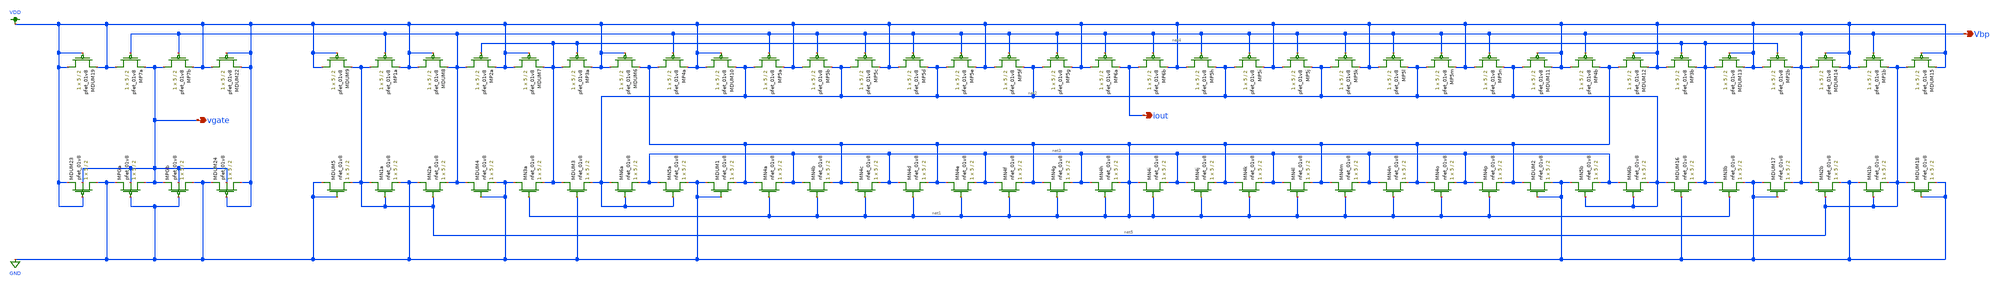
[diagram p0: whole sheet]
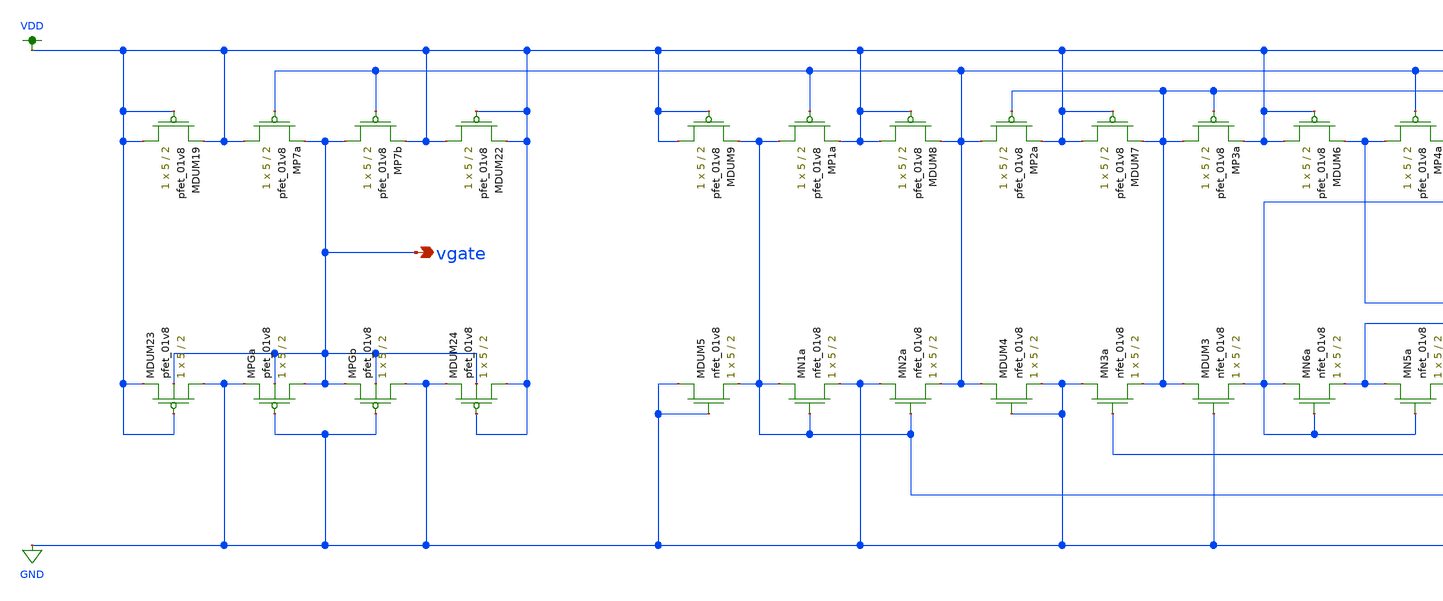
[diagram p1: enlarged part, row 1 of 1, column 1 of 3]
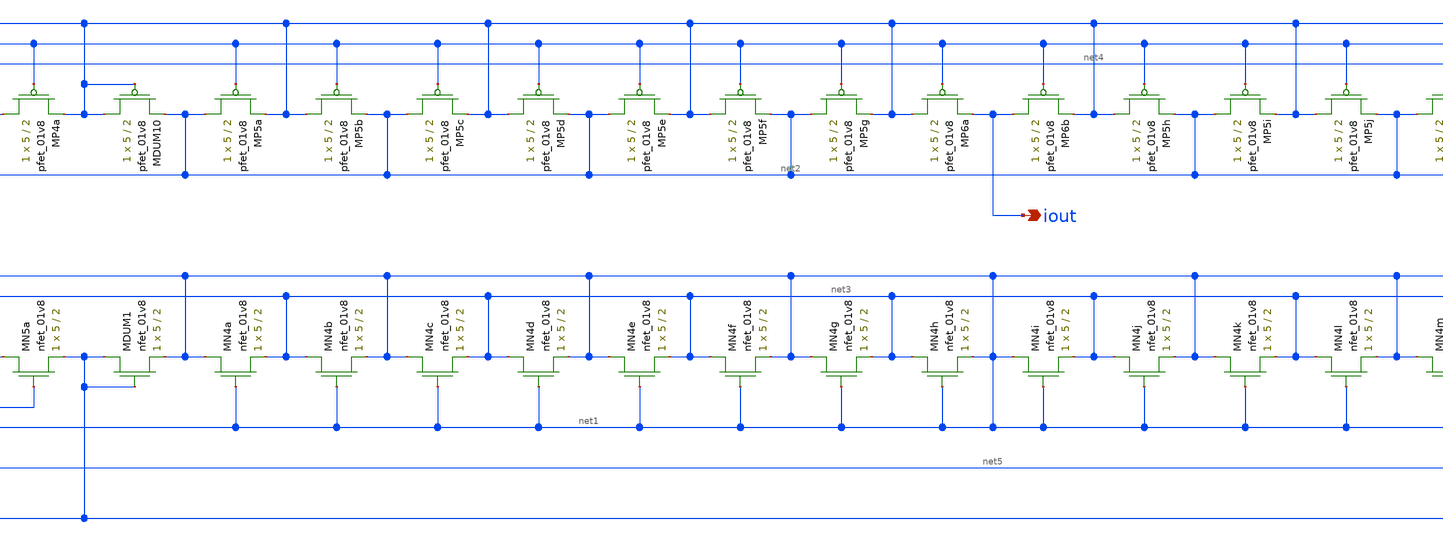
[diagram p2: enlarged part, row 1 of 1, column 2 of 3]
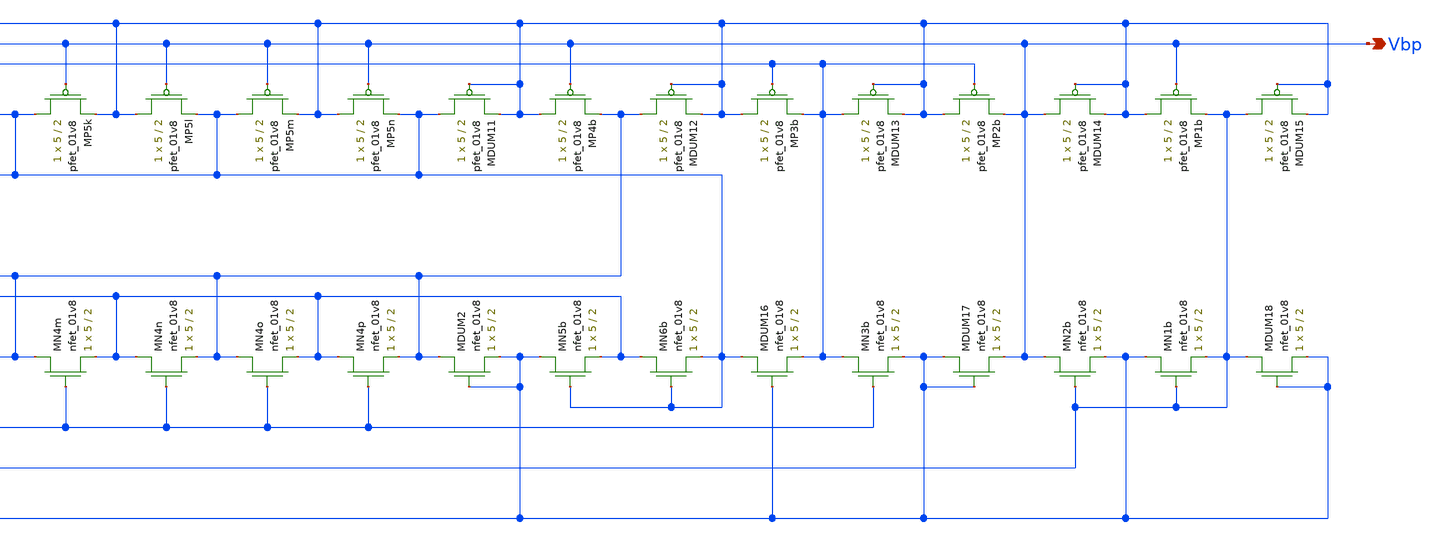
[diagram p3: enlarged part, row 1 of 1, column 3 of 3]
** sch_path: schematic/bias_current_LDS.sch
**.subckt bias_current_LDS iout Vbp vgate
*.opin iout
*.opin Vbp
*.opin vgate
XMP1a net5 Vbp VDD VDD sky130_fd_pr__pfet_01v8 L=2 W=5 nf=1 ad='int((nf+1)/2) * W/nf * 0.29' as='int((nf+2)/2) * W/nf * 0.29'
+ pd='2*int((nf+1)/2) * (W/nf + 0.29)' ps='2*int((nf+2)/2) * (W/nf + 0.29)' nrd='0.29 / W' nrs='0.29 / W'
+ sa=0 sb=0 sd=0 mult=1 m=1
XMP1b VDD Vbp net5 VDD sky130_fd_pr__pfet_01v8 L=2 W=5 nf=1 ad='int((nf+1)/2) * W/nf * 0.29' as='int((nf+2)/2) * W/nf * 0.29'
+ pd='2*int((nf+1)/2) * (W/nf + 0.29)' ps='2*int((nf+2)/2) * (W/nf + 0.29)' nrd='0.29 / W' nrs='0.29 / W'
+ sa=0 sb=0 sd=0 mult=1 m=1
XMP2a Vbp net4 VDD VDD sky130_fd_pr__pfet_01v8 L=2 W=5 nf=1 ad='int((nf+1)/2) * W/nf * 0.29' as='int((nf+2)/2) * W/nf * 0.29'
+ pd='2*int((nf+1)/2) * (W/nf + 0.29)' ps='2*int((nf+2)/2) * (W/nf + 0.29)' nrd='0.29 / W' nrs='0.29 / W'
+ sa=0 sb=0 sd=0 mult=1 m=1
XMP2b VDD net4 Vbp VDD sky130_fd_pr__pfet_01v8 L=2 W=5 nf=1 ad='int((nf+1)/2) * W/nf * 0.29' as='int((nf+2)/2) * W/nf * 0.29'
+ pd='2*int((nf+1)/2) * (W/nf + 0.29)' ps='2*int((nf+2)/2) * (W/nf + 0.29)' nrd='0.29 / W' nrs='0.29 / W'
+ sa=0 sb=0 sd=0 mult=1 m=1
XMP3a net4 net4 VDD VDD sky130_fd_pr__pfet_01v8 L=2 W=5 nf=1 ad='int((nf+1)/2) * W/nf * 0.29' as='int((nf+2)/2) * W/nf * 0.29'
+ pd='2*int((nf+1)/2) * (W/nf + 0.29)' ps='2*int((nf+2)/2) * (W/nf + 0.29)' nrd='0.29 / W' nrs='0.29 / W'
+ sa=0 sb=0 sd=0 mult=1 m=1
XMP3b VDD net4 net4 VDD sky130_fd_pr__pfet_01v8 L=2 W=5 nf=1 ad='int((nf+1)/2) * W/nf * 0.29' as='int((nf+2)/2) * W/nf * 0.29'
+ pd='2*int((nf+1)/2) * (W/nf + 0.29)' ps='2*int((nf+2)/2) * (W/nf + 0.29)' nrd='0.29 / W' nrs='0.29 / W'
+ sa=0 sb=0 sd=0 mult=1 m=1
XMP4a net1 Vbp VDD VDD sky130_fd_pr__pfet_01v8 L=2 W=5 nf=1 ad='int((nf+1)/2) * W/nf * 0.29' as='int((nf+2)/2) * W/nf * 0.29'
+ pd='2*int((nf+1)/2) * (W/nf + 0.29)' ps='2*int((nf+2)/2) * (W/nf + 0.29)' nrd='0.29 / W' nrs='0.29 / W'
+ sa=0 sb=0 sd=0 mult=1 m=1
XMP4b VDD Vbp net1 VDD sky130_fd_pr__pfet_01v8 L=2 W=5 nf=1 ad='int((nf+1)/2) * W/nf * 0.29' as='int((nf+2)/2) * W/nf * 0.29'
+ pd='2*int((nf+1)/2) * (W/nf + 0.29)' ps='2*int((nf+2)/2) * (W/nf + 0.29)' nrd='0.29 / W' nrs='0.29 / W'
+ sa=0 sb=0 sd=0 mult=1 m=1
XMN1a net5 net5 GND GND sky130_fd_pr__nfet_01v8 L=2 W=5 nf=1 ad='int((nf+1)/2) * W/nf * 0.29' as='int((nf+2)/2) * W/nf * 0.29'
+ pd='2*int((nf+1)/2) * (W/nf + 0.29)' ps='2*int((nf+2)/2) * (W/nf + 0.29)' nrd='0.29 / W' nrs='0.29 / W'
+ sa=0 sb=0 sd=0 mult=1 m=1
XMN1b GND net5 net5 GND sky130_fd_pr__nfet_01v8 L=2 W=5 nf=1 ad='int((nf+1)/2) * W/nf * 0.29' as='int((nf+2)/2) * W/nf * 0.29'
+ pd='2*int((nf+1)/2) * (W/nf + 0.29)' ps='2*int((nf+2)/2) * (W/nf + 0.29)' nrd='0.29 / W' nrs='0.29 / W'
+ sa=0 sb=0 sd=0 mult=1 m=1
XMN2a GND net5 Vbp GND sky130_fd_pr__nfet_01v8 L=2 W=5 nf=1 ad='int((nf+1)/2) * W/nf * 0.29' as='int((nf+2)/2) * W/nf * 0.29'
+ pd='2*int((nf+1)/2) * (W/nf + 0.29)' ps='2*int((nf+2)/2) * (W/nf + 0.29)' nrd='0.29 / W' nrs='0.29 / W'
+ sa=0 sb=0 sd=0 mult=1 m=1
XMN2b Vbp net5 GND GND sky130_fd_pr__nfet_01v8 L=2 W=5 nf=1 ad='int((nf+1)/2) * W/nf * 0.29' as='int((nf+2)/2) * W/nf * 0.29'
+ pd='2*int((nf+1)/2) * (W/nf + 0.29)' ps='2*int((nf+2)/2) * (W/nf + 0.29)' nrd='0.29 / W' nrs='0.29 / W'
+ sa=0 sb=0 sd=0 mult=1 m=1
XMN3a GND net1 net4 GND sky130_fd_pr__nfet_01v8 L=2 W=5 nf=1 ad='int((nf+1)/2) * W/nf * 0.29' as='int((nf+2)/2) * W/nf * 0.29'
+ pd='2*int((nf+1)/2) * (W/nf + 0.29)' ps='2*int((nf+2)/2) * (W/nf + 0.29)' nrd='0.29 / W' nrs='0.29 / W'
+ sa=0 sb=0 sd=0 mult=1 m=1
XMN3b net4 net1 GND GND sky130_fd_pr__nfet_01v8 L=2 W=5 nf=1 ad='int((nf+1)/2) * W/nf * 0.29' as='int((nf+2)/2) * W/nf * 0.29'
+ pd='2*int((nf+1)/2) * (W/nf + 0.29)' ps='2*int((nf+2)/2) * (W/nf + 0.29)' nrd='0.29 / W' nrs='0.29 / W'
+ sa=0 sb=0 sd=0 mult=1 m=1
XMN5a net3 net2 GND GND sky130_fd_pr__nfet_01v8 L=2 W=5 nf=1 ad='int((nf+1)/2) * W/nf * 0.29' as='int((nf+2)/2) * W/nf * 0.29'
+ pd='2*int((nf+1)/2) * (W/nf + 0.29)' ps='2*int((nf+2)/2) * (W/nf + 0.29)' nrd='0.29 / W' nrs='0.29 / W'
+ sa=0 sb=0 sd=0 mult=1 m=1
XMN5b GND net2 net3 GND sky130_fd_pr__nfet_01v8 L=2 W=5 nf=1 ad='int((nf+1)/2) * W/nf * 0.29' as='int((nf+2)/2) * W/nf * 0.29'
+ pd='2*int((nf+1)/2) * (W/nf + 0.29)' ps='2*int((nf+2)/2) * (W/nf + 0.29)' nrd='0.29 / W' nrs='0.29 / W'
+ sa=0 sb=0 sd=0 mult=1 m=1
XMN6a net2 net2 net3 GND sky130_fd_pr__nfet_01v8 L=2 W=5 nf=1 ad='int((nf+1)/2) * W/nf * 0.29' as='int((nf+2)/2) * W/nf * 0.29'
+ pd='2*int((nf+1)/2) * (W/nf + 0.29)' ps='2*int((nf+2)/2) * (W/nf + 0.29)' nrd='0.29 / W' nrs='0.29 / W'
+ sa=0 sb=0 sd=0 mult=1 m=1
XMN6b net3 net2 net2 GND sky130_fd_pr__nfet_01v8 L=2 W=5 nf=1 ad='int((nf+1)/2) * W/nf * 0.29' as='int((nf+2)/2) * W/nf * 0.29'
+ pd='2*int((nf+1)/2) * (W/nf + 0.29)' ps='2*int((nf+2)/2) * (W/nf + 0.29)' nrd='0.29 / W' nrs='0.29 / W'
+ sa=0 sb=0 sd=0 mult=1 m=1
XMP5g net2 Vbp VDD VDD sky130_fd_pr__pfet_01v8 L=2 W=5 nf=1 ad='int((nf+1)/2) * W/nf * 0.29' as='int((nf+2)/2) * W/nf * 0.29'
+ pd='2*int((nf+1)/2) * (W/nf + 0.29)' ps='2*int((nf+2)/2) * (W/nf + 0.29)' nrd='0.29 / W' nrs='0.29 / W'
+ sa=0 sb=0 sd=0 mult=1 m=1
XMP5h VDD Vbp net2 VDD sky130_fd_pr__pfet_01v8 L=2 W=5 nf=1 ad='int((nf+1)/2) * W/nf * 0.29' as='int((nf+2)/2) * W/nf * 0.29'
+ pd='2*int((nf+1)/2) * (W/nf + 0.29)' ps='2*int((nf+2)/2) * (W/nf + 0.29)' nrd='0.29 / W' nrs='0.29 / W'
+ sa=0 sb=0 sd=0 mult=1 m=1
XMP5a net2 Vbp VDD VDD sky130_fd_pr__pfet_01v8 L=2 W=5 nf=1 ad='int((nf+1)/2) * W/nf * 0.29' as='int((nf+2)/2) * W/nf * 0.29'
+ pd='2*int((nf+1)/2) * (W/nf + 0.29)' ps='2*int((nf+2)/2) * (W/nf + 0.29)' nrd='0.29 / W' nrs='0.29 / W'
+ sa=0 sb=0 sd=0 mult=1 m=1
XMP5b VDD Vbp net2 VDD sky130_fd_pr__pfet_01v8 L=2 W=5 nf=1 ad='int((nf+1)/2) * W/nf * 0.29' as='int((nf+2)/2) * W/nf * 0.29'
+ pd='2*int((nf+1)/2) * (W/nf + 0.29)' ps='2*int((nf+2)/2) * (W/nf + 0.29)' nrd='0.29 / W' nrs='0.29 / W'
+ sa=0 sb=0 sd=0 mult=1 m=1
XMP5c net2 Vbp VDD VDD sky130_fd_pr__pfet_01v8 L=2 W=5 nf=1 ad='int((nf+1)/2) * W/nf * 0.29' as='int((nf+2)/2) * W/nf * 0.29'
+ pd='2*int((nf+1)/2) * (W/nf + 0.29)' ps='2*int((nf+2)/2) * (W/nf + 0.29)' nrd='0.29 / W' nrs='0.29 / W'
+ sa=0 sb=0 sd=0 mult=1 m=1
XMP5d VDD Vbp net2 VDD sky130_fd_pr__pfet_01v8 L=2 W=5 nf=1 ad='int((nf+1)/2) * W/nf * 0.29' as='int((nf+2)/2) * W/nf * 0.29'
+ pd='2*int((nf+1)/2) * (W/nf + 0.29)' ps='2*int((nf+2)/2) * (W/nf + 0.29)' nrd='0.29 / W' nrs='0.29 / W'
+ sa=0 sb=0 sd=0 mult=1 m=1
XMP5e net2 Vbp VDD VDD sky130_fd_pr__pfet_01v8 L=2 W=5 nf=1 ad='int((nf+1)/2) * W/nf * 0.29' as='int((nf+2)/2) * W/nf * 0.29'
+ pd='2*int((nf+1)/2) * (W/nf + 0.29)' ps='2*int((nf+2)/2) * (W/nf + 0.29)' nrd='0.29 / W' nrs='0.29 / W'
+ sa=0 sb=0 sd=0 mult=1 m=1
XMP5f VDD Vbp net2 VDD sky130_fd_pr__pfet_01v8 L=2 W=5 nf=1 ad='int((nf+1)/2) * W/nf * 0.29' as='int((nf+2)/2) * W/nf * 0.29'
+ pd='2*int((nf+1)/2) * (W/nf + 0.29)' ps='2*int((nf+2)/2) * (W/nf + 0.29)' nrd='0.29 / W' nrs='0.29 / W'
+ sa=0 sb=0 sd=0 mult=1 m=1
XMP5i net2 Vbp VDD VDD sky130_fd_pr__pfet_01v8 L=2 W=5 nf=1 ad='int((nf+1)/2) * W/nf * 0.29' as='int((nf+2)/2) * W/nf * 0.29'
+ pd='2*int((nf+1)/2) * (W/nf + 0.29)' ps='2*int((nf+2)/2) * (W/nf + 0.29)' nrd='0.29 / W' nrs='0.29 / W'
+ sa=0 sb=0 sd=0 mult=1 m=1
XMP5j VDD Vbp net2 VDD sky130_fd_pr__pfet_01v8 L=2 W=5 nf=1 ad='int((nf+1)/2) * W/nf * 0.29' as='int((nf+2)/2) * W/nf * 0.29'
+ pd='2*int((nf+1)/2) * (W/nf + 0.29)' ps='2*int((nf+2)/2) * (W/nf + 0.29)' nrd='0.29 / W' nrs='0.29 / W'
+ sa=0 sb=0 sd=0 mult=1 m=1
XMP5k net2 Vbp VDD VDD sky130_fd_pr__pfet_01v8 L=2 W=5 nf=1 ad='int((nf+1)/2) * W/nf * 0.29' as='int((nf+2)/2) * W/nf * 0.29'
+ pd='2*int((nf+1)/2) * (W/nf + 0.29)' ps='2*int((nf+2)/2) * (W/nf + 0.29)' nrd='0.29 / W' nrs='0.29 / W'
+ sa=0 sb=0 sd=0 mult=1 m=1
XMP5l VDD Vbp net2 VDD sky130_fd_pr__pfet_01v8 L=2 W=5 nf=1 ad='int((nf+1)/2) * W/nf * 0.29' as='int((nf+2)/2) * W/nf * 0.29'
+ pd='2*int((nf+1)/2) * (W/nf + 0.29)' ps='2*int((nf+2)/2) * (W/nf + 0.29)' nrd='0.29 / W' nrs='0.29 / W'
+ sa=0 sb=0 sd=0 mult=1 m=1
XMP5m net2 Vbp VDD VDD sky130_fd_pr__pfet_01v8 L=2 W=5 nf=1 ad='int((nf+1)/2) * W/nf * 0.29' as='int((nf+2)/2) * W/nf * 0.29'
+ pd='2*int((nf+1)/2) * (W/nf + 0.29)' ps='2*int((nf+2)/2) * (W/nf + 0.29)' nrd='0.29 / W' nrs='0.29 / W'
+ sa=0 sb=0 sd=0 mult=1 m=1
XMP5n VDD Vbp net2 VDD sky130_fd_pr__pfet_01v8 L=2 W=5 nf=1 ad='int((nf+1)/2) * W/nf * 0.29' as='int((nf+2)/2) * W/nf * 0.29'
+ pd='2*int((nf+1)/2) * (W/nf + 0.29)' ps='2*int((nf+2)/2) * (W/nf + 0.29)' nrd='0.29 / W' nrs='0.29 / W'
+ sa=0 sb=0 sd=0 mult=1 m=1
XMP7a VDD Vbp vgate VDD sky130_fd_pr__pfet_01v8 L=2 W=5 nf=1 ad='int((nf+1)/2) * W/nf * 0.29' as='int((nf+2)/2) * W/nf * 0.29'
+ pd='2*int((nf+1)/2) * (W/nf + 0.29)' ps='2*int((nf+2)/2) * (W/nf + 0.29)' nrd='0.29 / W' nrs='0.29 / W'
+ sa=0 sb=0 sd=0 mult=1 m=1
XMDUM1 GND GND net1 GND sky130_fd_pr__nfet_01v8 L=2 W=5 nf=1 ad='int((nf+1)/2) * W/nf * 0.29' as='int((nf+2)/2) * W/nf * 0.29'
+ pd='2*int((nf+1)/2) * (W/nf + 0.29)' ps='2*int((nf+2)/2) * (W/nf + 0.29)' nrd='0.29 / W' nrs='0.29 / W'
+ sa=0 sb=0 sd=0 mult=1 m=1
XMN4a net1 net1 net3 GND sky130_fd_pr__nfet_01v8 L=2 W=5 nf=1 ad='int((nf+1)/2) * W/nf * 0.29' as='int((nf+2)/2) * W/nf * 0.29'
+ pd='2*int((nf+1)/2) * (W/nf + 0.29)' ps='2*int((nf+2)/2) * (W/nf + 0.29)' nrd='0.29 / W' nrs='0.29 / W'
+ sa=0 sb=0 sd=0 mult=1 m=1
XMN4b net3 net1 net1 GND sky130_fd_pr__nfet_01v8 L=2 W=5 nf=1 ad='int((nf+1)/2) * W/nf * 0.29' as='int((nf+2)/2) * W/nf * 0.29'
+ pd='2*int((nf+1)/2) * (W/nf + 0.29)' ps='2*int((nf+2)/2) * (W/nf + 0.29)' nrd='0.29 / W' nrs='0.29 / W'
+ sa=0 sb=0 sd=0 mult=1 m=1
XMN4c net1 net1 net3 GND sky130_fd_pr__nfet_01v8 L=2 W=5 nf=1 ad='int((nf+1)/2) * W/nf * 0.29' as='int((nf+2)/2) * W/nf * 0.29'
+ pd='2*int((nf+1)/2) * (W/nf + 0.29)' ps='2*int((nf+2)/2) * (W/nf + 0.29)' nrd='0.29 / W' nrs='0.29 / W'
+ sa=0 sb=0 sd=0 mult=1 m=1
XMN4d net3 net1 net1 GND sky130_fd_pr__nfet_01v8 L=2 W=5 nf=1 ad='int((nf+1)/2) * W/nf * 0.29' as='int((nf+2)/2) * W/nf * 0.29'
+ pd='2*int((nf+1)/2) * (W/nf + 0.29)' ps='2*int((nf+2)/2) * (W/nf + 0.29)' nrd='0.29 / W' nrs='0.29 / W'
+ sa=0 sb=0 sd=0 mult=1 m=1
XMN4e net1 net1 net3 GND sky130_fd_pr__nfet_01v8 L=2 W=5 nf=1 ad='int((nf+1)/2) * W/nf * 0.29' as='int((nf+2)/2) * W/nf * 0.29'
+ pd='2*int((nf+1)/2) * (W/nf + 0.29)' ps='2*int((nf+2)/2) * (W/nf + 0.29)' nrd='0.29 / W' nrs='0.29 / W'
+ sa=0 sb=0 sd=0 mult=1 m=1
XMN4f net3 net1 net1 GND sky130_fd_pr__nfet_01v8 L=2 W=5 nf=1 ad='int((nf+1)/2) * W/nf * 0.29' as='int((nf+2)/2) * W/nf * 0.29'
+ pd='2*int((nf+1)/2) * (W/nf + 0.29)' ps='2*int((nf+2)/2) * (W/nf + 0.29)' nrd='0.29 / W' nrs='0.29 / W'
+ sa=0 sb=0 sd=0 mult=1 m=1
XMN4i net1 net1 net3 GND sky130_fd_pr__nfet_01v8 L=2 W=5 nf=1 ad='int((nf+1)/2) * W/nf * 0.29' as='int((nf+2)/2) * W/nf * 0.29'
+ pd='2*int((nf+1)/2) * (W/nf + 0.29)' ps='2*int((nf+2)/2) * (W/nf + 0.29)' nrd='0.29 / W' nrs='0.29 / W'
+ sa=0 sb=0 sd=0 mult=1 m=1
XMN4g net1 net1 net3 GND sky130_fd_pr__nfet_01v8 L=2 W=5 nf=1 ad='int((nf+1)/2) * W/nf * 0.29' as='int((nf+2)/2) * W/nf * 0.29'
+ pd='2*int((nf+1)/2) * (W/nf + 0.29)' ps='2*int((nf+2)/2) * (W/nf + 0.29)' nrd='0.29 / W' nrs='0.29 / W'
+ sa=0 sb=0 sd=0 mult=1 m=1
XMN4h net3 net1 net1 GND sky130_fd_pr__nfet_01v8 L=2 W=5 nf=1 ad='int((nf+1)/2) * W/nf * 0.29' as='int((nf+2)/2) * W/nf * 0.29'
+ pd='2*int((nf+1)/2) * (W/nf + 0.29)' ps='2*int((nf+2)/2) * (W/nf + 0.29)' nrd='0.29 / W' nrs='0.29 / W'
+ sa=0 sb=0 sd=0 mult=1 m=1
XMN4j net3 net1 net1 GND sky130_fd_pr__nfet_01v8 L=2 W=5 nf=1 ad='int((nf+1)/2) * W/nf * 0.29' as='int((nf+2)/2) * W/nf * 0.29'
+ pd='2*int((nf+1)/2) * (W/nf + 0.29)' ps='2*int((nf+2)/2) * (W/nf + 0.29)' nrd='0.29 / W' nrs='0.29 / W'
+ sa=0 sb=0 sd=0 mult=1 m=1
XMN4k net1 net1 net3 GND sky130_fd_pr__nfet_01v8 L=2 W=5 nf=1 ad='int((nf+1)/2) * W/nf * 0.29' as='int((nf+2)/2) * W/nf * 0.29'
+ pd='2*int((nf+1)/2) * (W/nf + 0.29)' ps='2*int((nf+2)/2) * (W/nf + 0.29)' nrd='0.29 / W' nrs='0.29 / W'
+ sa=0 sb=0 sd=0 mult=1 m=1
XMN4l net3 net1 net1 GND sky130_fd_pr__nfet_01v8 L=2 W=5 nf=1 ad='int((nf+1)/2) * W/nf * 0.29' as='int((nf+2)/2) * W/nf * 0.29'
+ pd='2*int((nf+1)/2) * (W/nf + 0.29)' ps='2*int((nf+2)/2) * (W/nf + 0.29)' nrd='0.29 / W' nrs='0.29 / W'
+ sa=0 sb=0 sd=0 mult=1 m=1
XMN4m net1 net1 net3 GND sky130_fd_pr__nfet_01v8 L=2 W=5 nf=1 ad='int((nf+1)/2) * W/nf * 0.29' as='int((nf+2)/2) * W/nf * 0.29'
+ pd='2*int((nf+1)/2) * (W/nf + 0.29)' ps='2*int((nf+2)/2) * (W/nf + 0.29)' nrd='0.29 / W' nrs='0.29 / W'
+ sa=0 sb=0 sd=0 mult=1 m=1
XMN4p net3 net1 net1 GND sky130_fd_pr__nfet_01v8 L=2 W=5 nf=1 ad='int((nf+1)/2) * W/nf * 0.29' as='int((nf+2)/2) * W/nf * 0.29'
+ pd='2*int((nf+1)/2) * (W/nf + 0.29)' ps='2*int((nf+2)/2) * (W/nf + 0.29)' nrd='0.29 / W' nrs='0.29 / W'
+ sa=0 sb=0 sd=0 mult=1 m=1
XMN4n net3 net1 net1 GND sky130_fd_pr__nfet_01v8 L=2 W=5 nf=1 ad='int((nf+1)/2) * W/nf * 0.29' as='int((nf+2)/2) * W/nf * 0.29'
+ pd='2*int((nf+1)/2) * (W/nf + 0.29)' ps='2*int((nf+2)/2) * (W/nf + 0.29)' nrd='0.29 / W' nrs='0.29 / W'
+ sa=0 sb=0 sd=0 mult=1 m=1
XMN4o net1 net1 net3 GND sky130_fd_pr__nfet_01v8 L=2 W=5 nf=1 ad='int((nf+1)/2) * W/nf * 0.29' as='int((nf+2)/2) * W/nf * 0.29'
+ pd='2*int((nf+1)/2) * (W/nf + 0.29)' ps='2*int((nf+2)/2) * (W/nf + 0.29)' nrd='0.29 / W' nrs='0.29 / W'
+ sa=0 sb=0 sd=0 mult=1 m=1
XMDUM2 net1 GND GND GND sky130_fd_pr__nfet_01v8 L=2 W=5 nf=1 ad='int((nf+1)/2) * W/nf * 0.29' as='int((nf+2)/2) * W/nf * 0.29'
+ pd='2*int((nf+1)/2) * (W/nf + 0.29)' ps='2*int((nf+2)/2) * (W/nf + 0.29)' nrd='0.29 / W' nrs='0.29 / W'
+ sa=0 sb=0 sd=0 mult=1 m=1
XMDUM3 net4 GND net2 GND sky130_fd_pr__nfet_01v8 L=2 W=5 nf=1 ad='int((nf+1)/2) * W/nf * 0.29' as='int((nf+2)/2) * W/nf * 0.29'
+ pd='2*int((nf+1)/2) * (W/nf + 0.29)' ps='2*int((nf+2)/2) * (W/nf + 0.29)' nrd='0.29 / W' nrs='0.29 / W'
+ sa=0 sb=0 sd=0 mult=1 m=1
XMDUM4 Vbp GND GND GND sky130_fd_pr__nfet_01v8 L=2 W=5 nf=1 ad='int((nf+1)/2) * W/nf * 0.29' as='int((nf+2)/2) * W/nf * 0.29'
+ pd='2*int((nf+1)/2) * (W/nf + 0.29)' ps='2*int((nf+2)/2) * (W/nf + 0.29)' nrd='0.29 / W' nrs='0.29 / W'
+ sa=0 sb=0 sd=0 mult=1 m=1
XMDUM5 GND GND net5 GND sky130_fd_pr__nfet_01v8 L=2 W=5 nf=1 ad='int((nf+1)/2) * W/nf * 0.29' as='int((nf+2)/2) * W/nf * 0.29'
+ pd='2*int((nf+1)/2) * (W/nf + 0.29)' ps='2*int((nf+2)/2) * (W/nf + 0.29)' nrd='0.29 / W' nrs='0.29 / W'
+ sa=0 sb=0 sd=0 mult=1 m=1
XMDUM6 VDD VDD net1 VDD sky130_fd_pr__pfet_01v8 L=2 W=5 nf=1 ad='int((nf+1)/2) * W/nf * 0.29' as='int((nf+2)/2) * W/nf * 0.29'
+ pd='2*int((nf+1)/2) * (W/nf + 0.29)' ps='2*int((nf+2)/2) * (W/nf + 0.29)' nrd='0.29 / W' nrs='0.29 / W'
+ sa=0 sb=0 sd=0 mult=1 m=1
XMDUM7 VDD VDD net4 VDD sky130_fd_pr__pfet_01v8 L=2 W=5 nf=1 ad='int((nf+1)/2) * W/nf * 0.29' as='int((nf+2)/2) * W/nf * 0.29'
+ pd='2*int((nf+1)/2) * (W/nf + 0.29)' ps='2*int((nf+2)/2) * (W/nf + 0.29)' nrd='0.29 / W' nrs='0.29 / W'
+ sa=0 sb=0 sd=0 mult=1 m=1
XMDUM8 VDD VDD Vbp VDD sky130_fd_pr__pfet_01v8 L=2 W=5 nf=1 ad='int((nf+1)/2) * W/nf * 0.29' as='int((nf+2)/2) * W/nf * 0.29'
+ pd='2*int((nf+1)/2) * (W/nf + 0.29)' ps='2*int((nf+2)/2) * (W/nf + 0.29)' nrd='0.29 / W' nrs='0.29 / W'
+ sa=0 sb=0 sd=0 mult=1 m=1
XMDUM9 VDD VDD net5 VDD sky130_fd_pr__pfet_01v8 L=2 W=5 nf=1 ad='int((nf+1)/2) * W/nf * 0.29' as='int((nf+2)/2) * W/nf * 0.29'
+ pd='2*int((nf+1)/2) * (W/nf + 0.29)' ps='2*int((nf+2)/2) * (W/nf + 0.29)' nrd='0.29 / W' nrs='0.29 / W'
+ sa=0 sb=0 sd=0 mult=1 m=1
XMDUM10 VDD VDD net2 VDD sky130_fd_pr__pfet_01v8 L=2 W=5 nf=1 ad='int((nf+1)/2) * W/nf * 0.29' as='int((nf+2)/2) * W/nf * 0.29'
+ pd='2*int((nf+1)/2) * (W/nf + 0.29)' ps='2*int((nf+2)/2) * (W/nf + 0.29)' nrd='0.29 / W' nrs='0.29 / W'
+ sa=0 sb=0 sd=0 mult=1 m=1
XMDUM11 net2 VDD VDD VDD sky130_fd_pr__pfet_01v8 L=2 W=5 nf=1 ad='int((nf+1)/2) * W/nf * 0.29' as='int((nf+2)/2) * W/nf * 0.29'
+ pd='2*int((nf+1)/2) * (W/nf + 0.29)' ps='2*int((nf+2)/2) * (W/nf + 0.29)' nrd='0.29 / W' nrs='0.29 / W'
+ sa=0 sb=0 sd=0 mult=1 m=1
XMP6a VDD Vbp iout VDD sky130_fd_pr__pfet_01v8 L=2 W=5 nf=1 ad='int((nf+1)/2) * W/nf * 0.29' as='int((nf+2)/2) * W/nf * 0.29'
+ pd='2*int((nf+1)/2) * (W/nf + 0.29)' ps='2*int((nf+2)/2) * (W/nf + 0.29)' nrd='0.29 / W' nrs='0.29 / W'
+ sa=0 sb=0 sd=0 mult=1 m=1
XMP6b iout Vbp VDD VDD sky130_fd_pr__pfet_01v8 L=2 W=5 nf=1 ad='int((nf+1)/2) * W/nf * 0.29' as='int((nf+2)/2) * W/nf * 0.29'
+ pd='2*int((nf+1)/2) * (W/nf + 0.29)' ps='2*int((nf+2)/2) * (W/nf + 0.29)' nrd='0.29 / W' nrs='0.29 / W'
+ sa=0 sb=0 sd=0 mult=1 m=1
XMDUM12 net1 VDD VDD VDD sky130_fd_pr__pfet_01v8 L=2 W=5 nf=1 ad='int((nf+1)/2) * W/nf * 0.29' as='int((nf+2)/2) * W/nf * 0.29'
+ pd='2*int((nf+1)/2) * (W/nf + 0.29)' ps='2*int((nf+2)/2) * (W/nf + 0.29)' nrd='0.29 / W' nrs='0.29 / W'
+ sa=0 sb=0 sd=0 mult=1 m=1
XMDUM13 net4 VDD VDD VDD sky130_fd_pr__pfet_01v8 L=2 W=5 nf=1 ad='int((nf+1)/2) * W/nf * 0.29' as='int((nf+2)/2) * W/nf * 0.29'
+ pd='2*int((nf+1)/2) * (W/nf + 0.29)' ps='2*int((nf+2)/2) * (W/nf + 0.29)' nrd='0.29 / W' nrs='0.29 / W'
+ sa=0 sb=0 sd=0 mult=1 m=1
XMDUM14 Vbp VDD VDD VDD sky130_fd_pr__pfet_01v8 L=2 W=5 nf=1 ad='int((nf+1)/2) * W/nf * 0.29' as='int((nf+2)/2) * W/nf * 0.29'
+ pd='2*int((nf+1)/2) * (W/nf + 0.29)' ps='2*int((nf+2)/2) * (W/nf + 0.29)' nrd='0.29 / W' nrs='0.29 / W'
+ sa=0 sb=0 sd=0 mult=1 m=1
XMDUM15 net5 VDD VDD VDD sky130_fd_pr__pfet_01v8 L=2 W=5 nf=1 ad='int((nf+1)/2) * W/nf * 0.29' as='int((nf+2)/2) * W/nf * 0.29'
+ pd='2*int((nf+1)/2) * (W/nf + 0.29)' ps='2*int((nf+2)/2) * (W/nf + 0.29)' nrd='0.29 / W' nrs='0.29 / W'
+ sa=0 sb=0 sd=0 mult=1 m=1
XMDUM16 net2 GND net4 GND sky130_fd_pr__nfet_01v8 L=2 W=5 nf=1 ad='int((nf+1)/2) * W/nf * 0.29' as='int((nf+2)/2) * W/nf * 0.29'
+ pd='2*int((nf+1)/2) * (W/nf + 0.29)' ps='2*int((nf+2)/2) * (W/nf + 0.29)' nrd='0.29 / W' nrs='0.29 / W'
+ sa=0 sb=0 sd=0 mult=1 m=1
XMDUM17 GND GND Vbp GND sky130_fd_pr__nfet_01v8 L=2 W=5 nf=1 ad='int((nf+1)/2) * W/nf * 0.29' as='int((nf+2)/2) * W/nf * 0.29'
+ pd='2*int((nf+1)/2) * (W/nf + 0.29)' ps='2*int((nf+2)/2) * (W/nf + 0.29)' nrd='0.29 / W' nrs='0.29 / W'
+ sa=0 sb=0 sd=0 mult=1 m=1
XMDUM18 net5 GND GND GND sky130_fd_pr__nfet_01v8 L=2 W=5 nf=1 ad='int((nf+1)/2) * W/nf * 0.29' as='int((nf+2)/2) * W/nf * 0.29'
+ pd='2*int((nf+1)/2) * (W/nf + 0.29)' ps='2*int((nf+2)/2) * (W/nf + 0.29)' nrd='0.29 / W' nrs='0.29 / W'
+ sa=0 sb=0 sd=0 mult=1 m=1
XMDUM19 VDD VDD VDD VDD sky130_fd_pr__pfet_01v8 L=2 W=5 nf=1 ad='int((nf+1)/2) * W/nf * 0.29' as='int((nf+2)/2) * W/nf * 0.29'
+ pd='2*int((nf+1)/2) * (W/nf + 0.29)' ps='2*int((nf+2)/2) * (W/nf + 0.29)' nrd='0.29 / W' nrs='0.29 / W'
+ sa=0 sb=0 sd=0 mult=1 m=1
XMPGa vgate GND GND vgate sky130_fd_pr__pfet_01v8 L=2 W=5 nf=1 ad='int((nf+1)/2) * W/nf * 0.29' as='int((nf+2)/2) * W/nf * 0.29'
+ pd='2*int((nf+1)/2) * (W/nf + 0.29)' ps='2*int((nf+2)/2) * (W/nf + 0.29)' nrd='0.29 / W' nrs='0.29 / W'
+ sa=0 sb=0 sd=0 mult=1 m=1
XMP7b vgate Vbp VDD VDD sky130_fd_pr__pfet_01v8 L=2 W=5 nf=1 ad='int((nf+1)/2) * W/nf * 0.29' as='int((nf+2)/2) * W/nf * 0.29'
+ pd='2*int((nf+1)/2) * (W/nf + 0.29)' ps='2*int((nf+2)/2) * (W/nf + 0.29)' nrd='0.29 / W' nrs='0.29 / W'
+ sa=0 sb=0 sd=0 mult=1 m=1
XMPGb GND GND vgate vgate sky130_fd_pr__pfet_01v8 L=2 W=5 nf=1 ad='int((nf+1)/2) * W/nf * 0.29' as='int((nf+2)/2) * W/nf * 0.29'
+ pd='2*int((nf+1)/2) * (W/nf + 0.29)' ps='2*int((nf+2)/2) * (W/nf + 0.29)' nrd='0.29 / W' nrs='0.29 / W'
+ sa=0 sb=0 sd=0 mult=1 m=1
XMDUM22 VDD VDD VDD VDD sky130_fd_pr__pfet_01v8 L=2 W=5 nf=1 ad='int((nf+1)/2) * W/nf * 0.29' as='int((nf+2)/2) * W/nf * 0.29'
+ pd='2*int((nf+1)/2) * (W/nf + 0.29)' ps='2*int((nf+2)/2) * (W/nf + 0.29)' nrd='0.29 / W' nrs='0.29 / W'
+ sa=0 sb=0 sd=0 mult=1 m=1
XMDUM23 GND VDD VDD vgate sky130_fd_pr__pfet_01v8 L=2 W=5 nf=1 ad='int((nf+1)/2) * W/nf * 0.29' as='int((nf+2)/2) * W/nf * 0.29'
+ pd='2*int((nf+1)/2) * (W/nf + 0.29)' ps='2*int((nf+2)/2) * (W/nf + 0.29)' nrd='0.29 / W' nrs='0.29 / W'
+ sa=0 sb=0 sd=0 mult=1 m=1
XMDUM24 VDD VDD GND vgate sky130_fd_pr__pfet_01v8 L=2 W=5 nf=1 ad='int((nf+1)/2) * W/nf * 0.29' as='int((nf+2)/2) * W/nf * 0.29'
+ pd='2*int((nf+1)/2) * (W/nf + 0.29)' ps='2*int((nf+2)/2) * (W/nf + 0.29)' nrd='0.29 / W' nrs='0.29 / W'
+ sa=0 sb=0 sd=0 mult=1 m=1
**.ends
.GLOBAL VDD
.GLOBAL GND
.end
